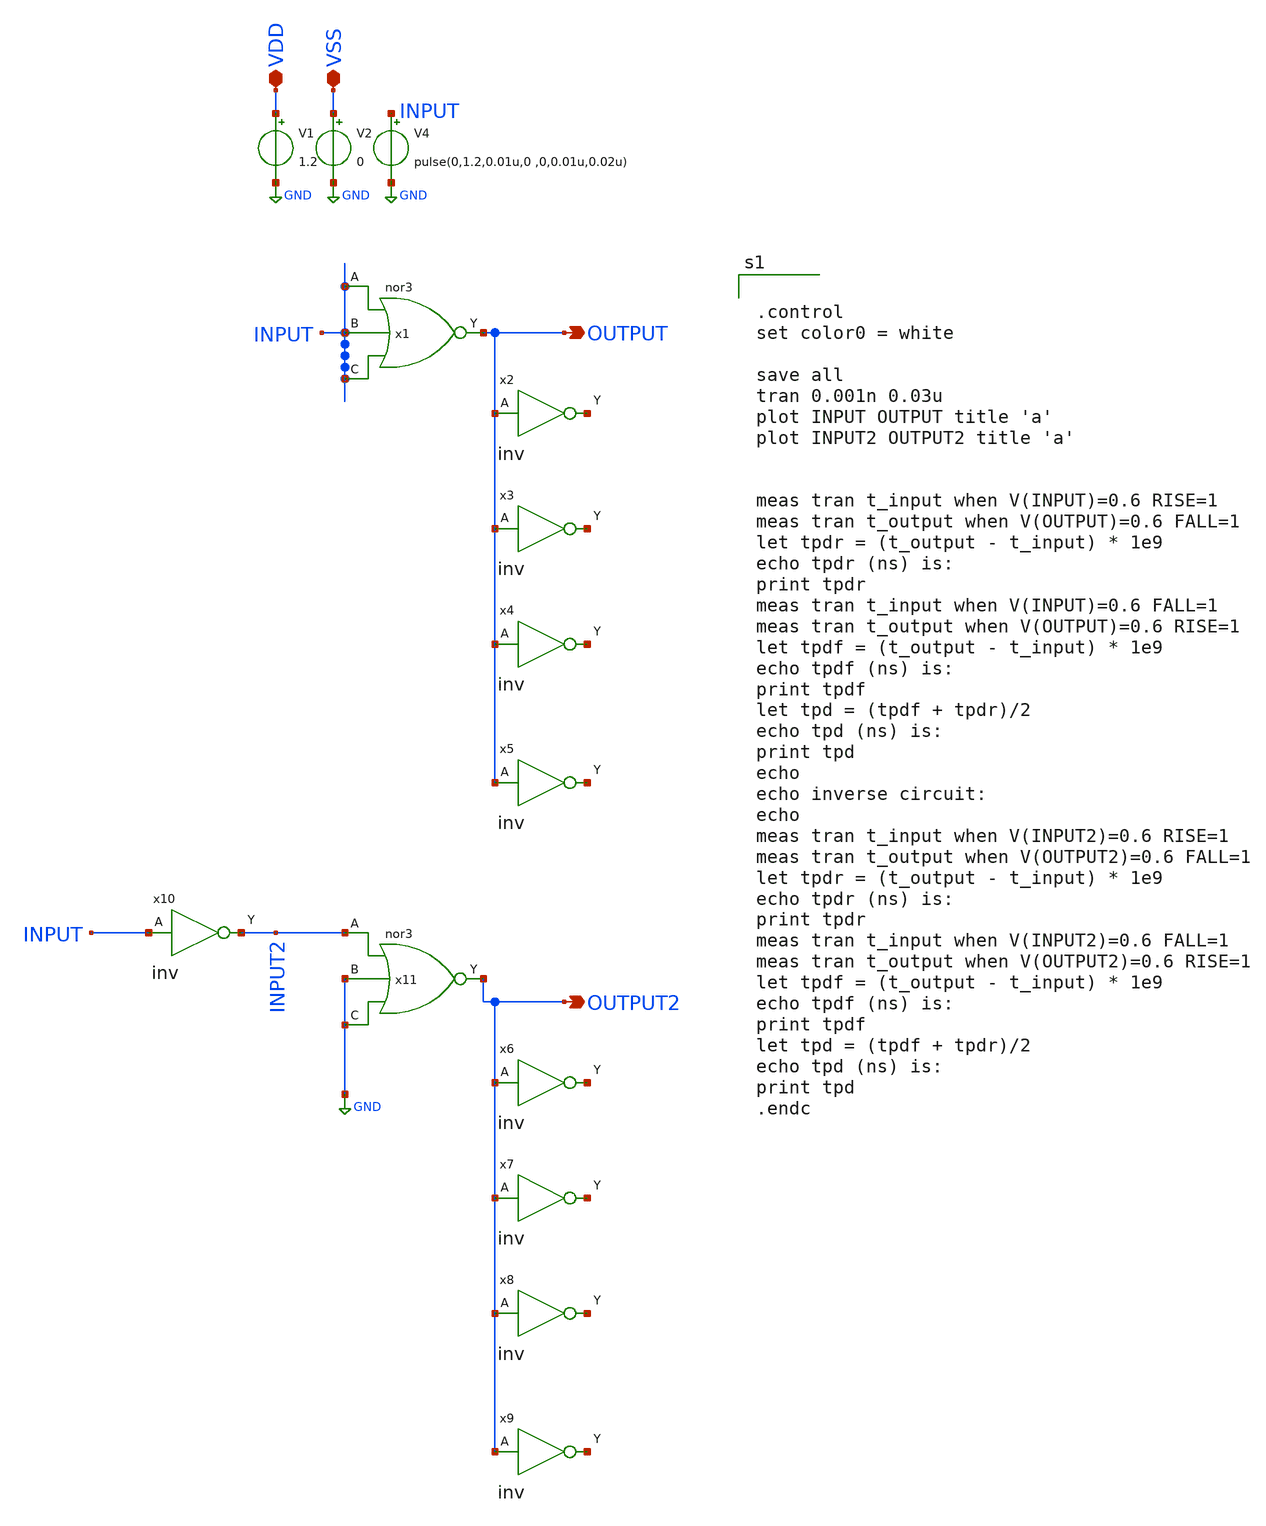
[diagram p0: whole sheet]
** sch_path: design/xschem/NOR/nor3_TB.sch
**.subckt nor3_TB OUTPUT VDD VSS OUTPUT2
*.opin OUTPUT
*.iopin VDD
*.iopin VSS
*.opin OUTPUT2
V1 VDD GND 1.2
V2 VSS GND 0
V4 INPUT GND pulse(0,1.2,0.01u,0 ,0,0.01u,0.02u)
x2 OUTPUT VSS VDD net1 inv
x3 OUTPUT VSS VDD net2 inv
x4 OUTPUT VSS VDD net3 inv
x5 OUTPUT VSS VDD net4 inv
x6 OUTPUT2 VSS VDD net5 inv
x7 OUTPUT2 VSS VDD net6 inv
x8 OUTPUT2 VSS VDD net7 inv
x9 OUTPUT2 VSS VDD net8 inv
x10 INPUT VSS VDD INPUT2 inv
x1 INPUT INPUT INPUT VSS VDD OUTPUT nor3
x11 INPUT2 GND GND VSS VDD OUTPUT2 nor3
**** begin user architecture code

** opencircuitdesign pdks install
.lib $::SKYWATER_MODELS/sky130.lib.spice tt_mm




.control
set color0 = white

save all
tran 0.001n 0.03u
plot INPUT OUTPUT title 'a'
plot INPUT2 OUTPUT2 title 'a'


meas tran t_input when V(INPUT)=0.6 RISE=1
meas tran t_output when V(OUTPUT)=0.6 FALL=1
let tpdr = (t_output - t_input) * 1e9
echo tpdr (ns) is:
print tpdr
meas tran t_input when V(INPUT)=0.6 FALL=1
meas tran t_output when V(OUTPUT)=0.6 RISE=1
let tpdf = (t_output - t_input) * 1e9
echo tpdf (ns) is:
print tpdf
let tpd = (tpdf + tpdr)/2
echo tpd (ns) is:
print tpd
echo
echo inverse circuit:
echo
meas tran t_input when V(INPUT2)=0.6 RISE=1
meas tran t_output when V(OUTPUT2)=0.6 FALL=1
let tpdr = (t_output - t_input) * 1e9
echo tpdr (ns) is:
print tpdr
meas tran t_input when V(INPUT2)=0.6 FALL=1
meas tran t_output when V(OUTPUT2)=0.6 RISE=1
let tpdf = (t_output - t_input) * 1e9
echo tpdf (ns) is:
print tpdf
let tpd = (tpdf + tpdr)/2
echo tpd (ns) is:
print tpd
.endc


**** end user architecture code
**.ends

* expanding   symbol:  INV/inv.sym # of pins=2
** sym_path: design/xschem/INV/inv.sym
** sch_path: design/xschem/INV/inv.sch
.subckt inv A VSS VDD Y
*.ipin A
*.opin Y
XM2 Y A VSS GND sky130_fd_pr__nfet_01v8 L=0.15 W=1 nf=1 ad='int((nf+1)/2) * W/nf * 0.29' as='int((nf+2)/2) * W/nf * 0.29'
+ pd='2*int((nf+1)/2) * (W/nf + 0.29)' ps='2*int((nf+2)/2) * (W/nf + 0.29)' nrd='0.29 / W' nrs='0.29 / W'
+ sa=0 sb=0 sd=0 mult=1 m=1
XM1 Y A VDD VDD sky130_fd_pr__pfet_01v8 L=0.15 W=3.21 nf=1 ad='int((nf+1)/2) * W/nf * 0.29' as='int((nf+2)/2) * W/nf * 0.29'
+ pd='2*int((nf+1)/2) * (W/nf + 0.29)' ps='2*int((nf+2)/2) * (W/nf + 0.29)' nrd='0.29 / W' nrs='0.29 / W'
+ sa=0 sb=0 sd=0 mult=1 m=1
.ends


* expanding   symbol:  NOR/nor3.sym # of pins=4
** sym_path: design/xschem/NOR/nor3.sym
** sch_path: design/xschem/NOR/nor3.sch
.subckt nor3 A B C VSS VDD Y
*.opin Y
*.ipin B
*.ipin C
*.ipin A
XM2 Y A VSS VSS sky130_fd_pr__nfet_01v8 L=0.15 W=1 nf=1 ad='int((nf+1)/2) * W/nf * 0.29' as='int((nf+2)/2) * W/nf * 0.29'
+ pd='2*int((nf+1)/2) * (W/nf + 0.29)' ps='2*int((nf+2)/2) * (W/nf + 0.29)' nrd='0.29 / W' nrs='0.29 / W'
+ sa=0 sb=0 sd=0 mult=1 m=1
XM3 Y B VSS VSS sky130_fd_pr__nfet_01v8 L=0.15 W=1 nf=1 ad='int((nf+1)/2) * W/nf * 0.29' as='int((nf+2)/2) * W/nf * 0.29'
+ pd='2*int((nf+1)/2) * (W/nf + 0.29)' ps='2*int((nf+2)/2) * (W/nf + 0.29)' nrd='0.29 / W' nrs='0.29 / W'
+ sa=0 sb=0 sd=0 mult=1 m=1
XM6 Y C VSS VSS sky130_fd_pr__nfet_01v8 L=0.15 W=1 nf=1 ad='int((nf+1)/2) * W/nf * 0.29' as='int((nf+2)/2) * W/nf * 0.29'
+ pd='2*int((nf+1)/2) * (W/nf + 0.29)' ps='2*int((nf+2)/2) * (W/nf + 0.29)' nrd='0.29 / W' nrs='0.29 / W'
+ sa=0 sb=0 sd=0 mult=1 m=1
XM1 net2 C VDD VDD sky130_fd_pr__pfet_01v8 L=0.15 W=9.63 nf=3 ad='int((nf+1)/2) * W/nf * 0.29' as='int((nf+2)/2) * W/nf * 0.29'
+ pd='2*int((nf+1)/2) * (W/nf + 0.29)' ps='2*int((nf+2)/2) * (W/nf + 0.29)' nrd='0.29 / W' nrs='0.29 / W'
+ sa=0 sb=0 sd=0 mult=1 m=1
XM4 net1 B net2 net2 sky130_fd_pr__pfet_01v8 L=0.15 W=9.63 nf=3 ad='int((nf+1)/2) * W/nf * 0.29' as='int((nf+2)/2) * W/nf * 0.29'
+ pd='2*int((nf+1)/2) * (W/nf + 0.29)' ps='2*int((nf+2)/2) * (W/nf + 0.29)' nrd='0.29 / W' nrs='0.29 / W'
+ sa=0 sb=0 sd=0 mult=1 m=1
XM5 Y A net1 net1 sky130_fd_pr__pfet_01v8 L=0.15 W=9.63 nf=3 ad='int((nf+1)/2) * W/nf * 0.29' as='int((nf+2)/2) * W/nf * 0.29'
+ pd='2*int((nf+1)/2) * (W/nf + 0.29)' ps='2*int((nf+2)/2) * (W/nf + 0.29)' nrd='0.29 / W' nrs='0.29 / W'
+ sa=0 sb=0 sd=0 mult=1 m=1
.ends

.GLOBAL GND
.end
